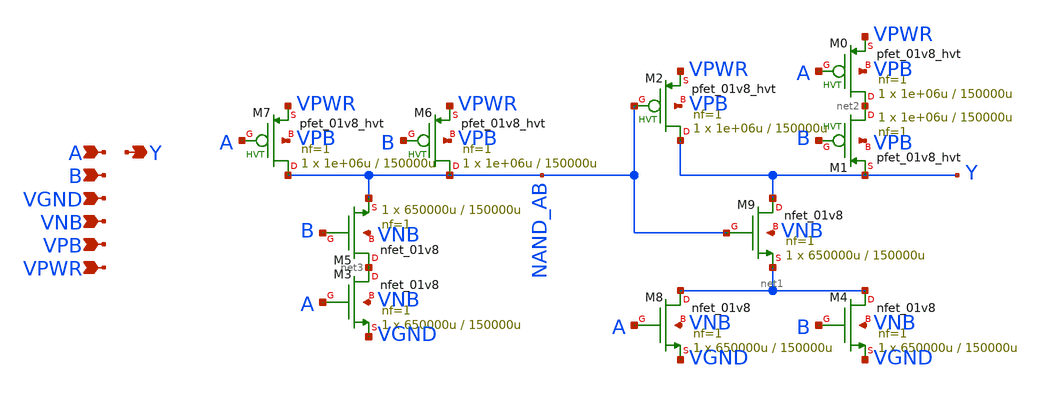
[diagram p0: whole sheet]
** sch_path: schematics/xnor2/sky130_fd_sc_hd__xnor2_1.sch
**.subckt sky130_fd_sc_hd__xnor2_1 A B VGND VNB VPB VPWR Y
*.ipin A
*.ipin B
*.ipin VGND
*.ipin VNB
*.ipin VPB
*.ipin VPWR
*.opin Y
XM0 net2 A VPWR VPB sky130_fd_pr__pfet_01v8_hvt L=150000u W=1e+06u nf=1 ad='int((1 + 1)/2) * 1e+06u / 1 * 0.29'
+ as='int((1 + 2)/2) * 1e+06u / 1 * 0.29' pd='2*int((1 + 1)/2) * (1e+06u / 1 + 0.29)' ps='2*int((1 + 2)/2) * (1e+06u / 1 + 0.29)'
+ nrd='0.29 / 1e+06u ' nrs='0.29 / 1e+06u ' sa=0 sb=0 sd=0 mult=1 m=1
XM7 NAND_AB A VPWR VPB sky130_fd_pr__pfet_01v8_hvt L=150000u W=1e+06u nf=1 ad='int((1 + 1)/2) * 1e+06u / 1 * 0.29'
+ as='int((1 + 2)/2) * 1e+06u / 1 * 0.29' pd='2*int((1 + 1)/2) * (1e+06u / 1 + 0.29)' ps='2*int((1 + 2)/2) * (1e+06u / 1 + 0.29)'
+ nrd='0.29 / 1e+06u ' nrs='0.29 / 1e+06u ' sa=0 sb=0 sd=0 mult=1 m=1
XM2 Y NAND_AB VPWR VPB sky130_fd_pr__pfet_01v8_hvt L=150000u W=1e+06u nf=1 ad='int((1 + 1)/2) * 1e+06u / 1 * 0.29'
+ as='int((1 + 2)/2) * 1e+06u / 1 * 0.29' pd='2*int((1 + 1)/2) * (1e+06u / 1 + 0.29)' ps='2*int((1 + 2)/2) * (1e+06u / 1 + 0.29)'
+ nrd='0.29 / 1e+06u ' nrs='0.29 / 1e+06u ' sa=0 sb=0 sd=0 mult=1 m=1
XM1 net2 B Y VPB sky130_fd_pr__pfet_01v8_hvt L=150000u W=1e+06u nf=1 ad='int((1 + 1)/2) * 1e+06u / 1 * 0.29'
+ as='int((1 + 2)/2) * 1e+06u / 1 * 0.29' pd='2*int((1 + 1)/2) * (1e+06u / 1 + 0.29)' ps='2*int((1 + 2)/2) * (1e+06u / 1 + 0.29)'
+ nrd='0.29 / 1e+06u ' nrs='0.29 / 1e+06u ' sa=0 sb=0 sd=0 mult=1 m=1
XM6 NAND_AB B VPWR VPB sky130_fd_pr__pfet_01v8_hvt L=150000u W=1e+06u nf=1 ad='int((1 + 1)/2) * 1e+06u / 1 * 0.29'
+ as='int((1 + 2)/2) * 1e+06u / 1 * 0.29' pd='2*int((1 + 1)/2) * (1e+06u / 1 + 0.29)' ps='2*int((1 + 2)/2) * (1e+06u / 1 + 0.29)'
+ nrd='0.29 / 1e+06u ' nrs='0.29 / 1e+06u ' sa=0 sb=0 sd=0 mult=1 m=1
XM3 net3 A VGND VNB sky130_fd_pr__nfet_01v8 L=150000u W=650000u nf=1 ad='int((1 + 1)/2) * 650000u / 1 * 0.29'
+ as='int((1 + 2)/2) * 650000u / 1 * 0.29' pd='2*int((1 + 1)/2) * (650000u / 1 + 0.29)' ps='2*int((1 + 2)/2) * (650000u / 1 + 0.29)'
+ nrd='0.29 / 650000u ' nrs='0.29 / 650000u ' sa=0 sb=0 sd=0 mult=1 m=1
XM8 net1 A VGND VNB sky130_fd_pr__nfet_01v8 L=150000u W=650000u nf=1 ad='int((1 + 1)/2) * 650000u / 1 * 0.29'
+ as='int((1 + 2)/2) * 650000u / 1 * 0.29' pd='2*int((1 + 1)/2) * (650000u / 1 + 0.29)' ps='2*int((1 + 2)/2) * (650000u / 1 + 0.29)'
+ nrd='0.29 / 650000u ' nrs='0.29 / 650000u ' sa=0 sb=0 sd=0 mult=1 m=1
XM9 Y NAND_AB net1 VNB sky130_fd_pr__nfet_01v8 L=150000u W=650000u nf=1 ad='int((1 + 1)/2) * 650000u / 1 * 0.29'
+ as='int((1 + 2)/2) * 650000u / 1 * 0.29' pd='2*int((1 + 1)/2) * (650000u / 1 + 0.29)' ps='2*int((1 + 2)/2) * (650000u / 1 + 0.29)'
+ nrd='0.29 / 650000u ' nrs='0.29 / 650000u ' sa=0 sb=0 sd=0 mult=1 m=1
XM4 net1 B VGND VNB sky130_fd_pr__nfet_01v8 L=150000u W=650000u nf=1 ad='int((1 + 1)/2) * 650000u / 1 * 0.29'
+ as='int((1 + 2)/2) * 650000u / 1 * 0.29' pd='2*int((1 + 1)/2) * (650000u / 1 + 0.29)' ps='2*int((1 + 2)/2) * (650000u / 1 + 0.29)'
+ nrd='0.29 / 650000u ' nrs='0.29 / 650000u ' sa=0 sb=0 sd=0 mult=1 m=1
XM5 net3 B NAND_AB VNB sky130_fd_pr__nfet_01v8 L=150000u W=650000u nf=1 ad='int((1 + 1)/2) * 650000u / 1 * 0.29'
+ as='int((1 + 2)/2) * 650000u / 1 * 0.29' pd='2*int((1 + 1)/2) * (650000u / 1 + 0.29)' ps='2*int((1 + 2)/2) * (650000u / 1 + 0.29)'
+ nrd='0.29 / 650000u ' nrs='0.29 / 650000u ' sa=0 sb=0 sd=0 mult=1 m=1
**.ends
.end
